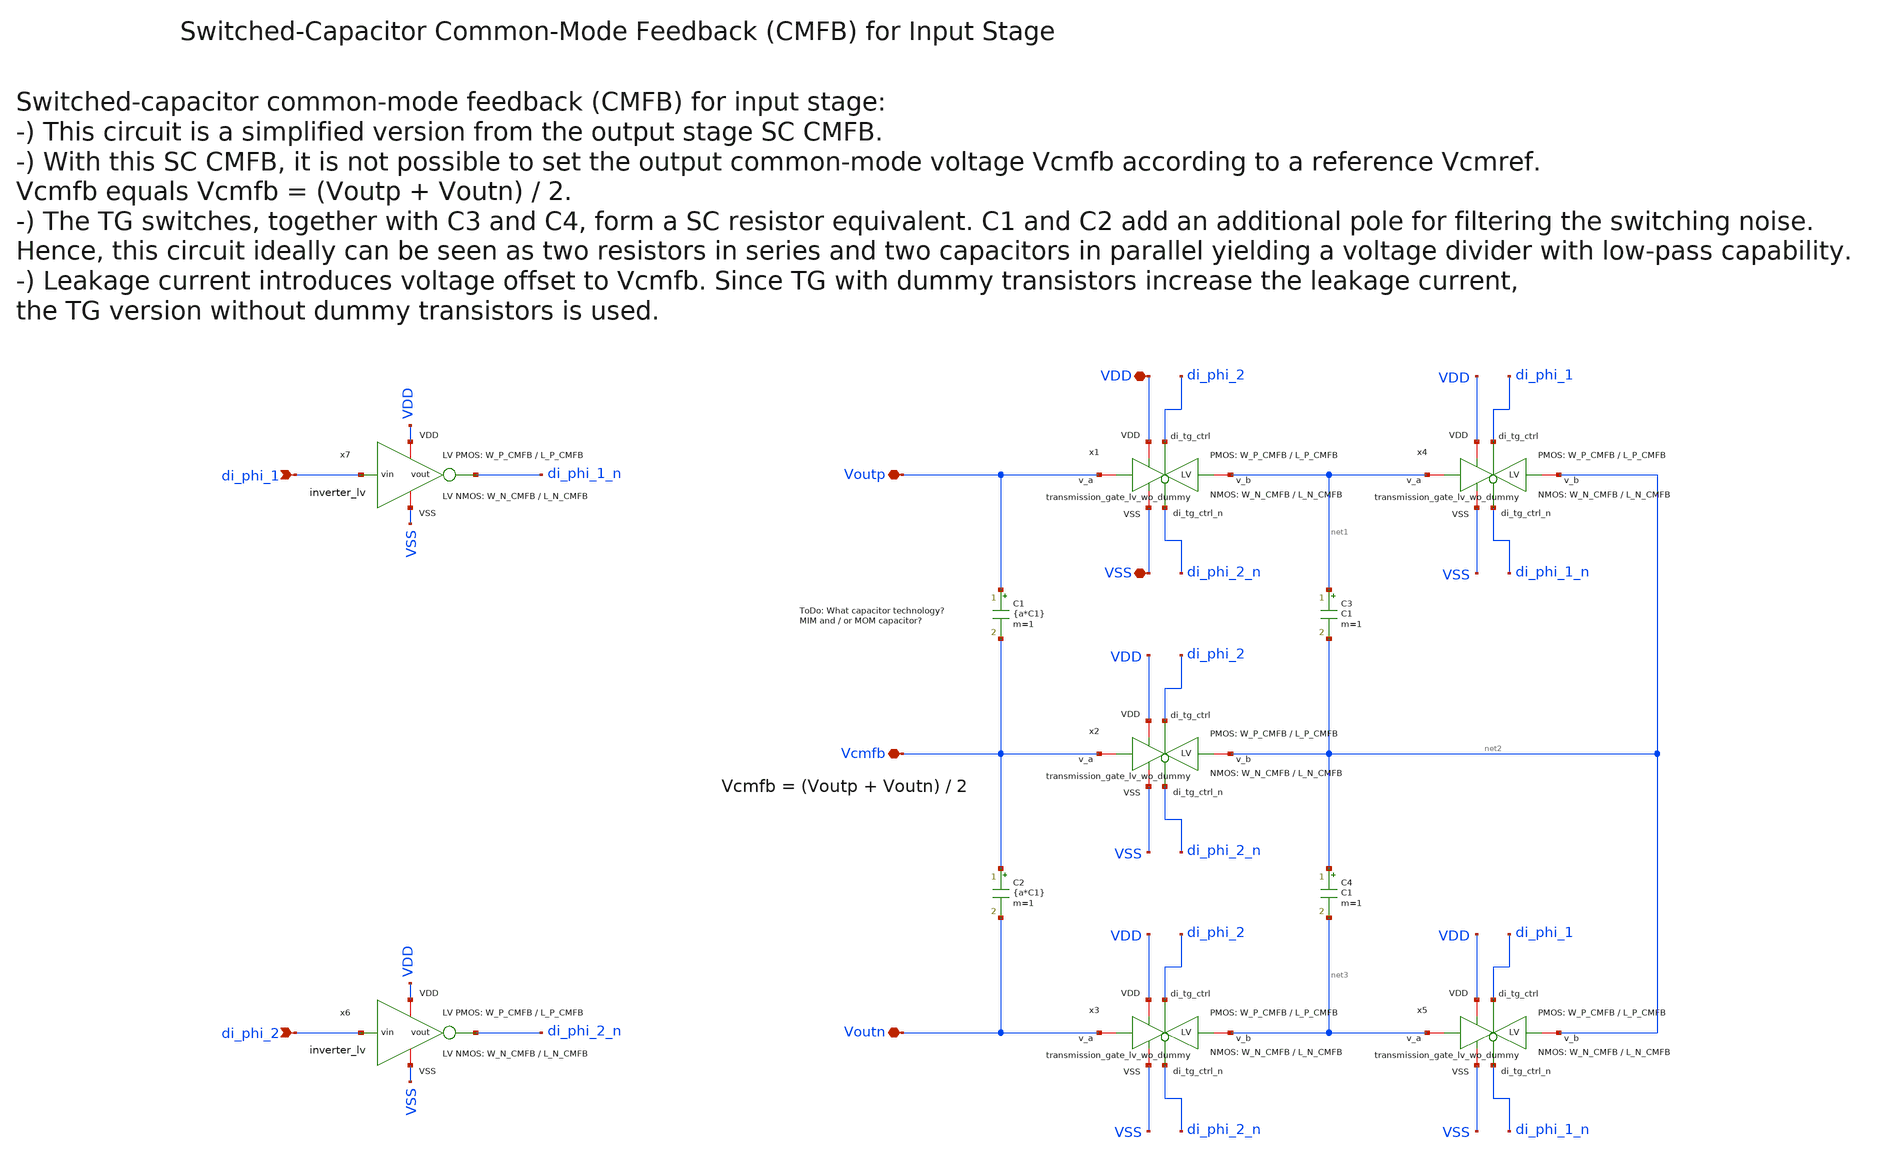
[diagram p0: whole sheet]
** sch_path: SG13G2_ATBS-ADC-main/xschem/bio_amplifier/amplifier_core/sc_cmfb/sc_cmfb_input.sch
**.subckt sc_cmfb_input VSS VDD Vcmfb Voutp Voutn di_phi_1 di_phi_2
*.iopin VSS
*.iopin VDD
*.iopin Vcmfb
*.iopin Voutp
*.iopin Voutn
*.ipin di_phi_1
*.ipin di_phi_2
x1 VDD di_phi_2 VSS net1 Voutp di_phi_2_n transmission_gate_lv_wo_dummy W_P=W_P_CMFB L_P=L_P_CMFB
+ W_N=W_N_CMFB L_N=L_N_CMFB
C1 Voutp Vcmfb {a*C1} m=1
x2 VDD di_phi_2 VSS net2 Vcmfb di_phi_2_n transmission_gate_lv_wo_dummy W_P=W_P_CMFB L_P=L_P_CMFB
+ W_N=W_N_CMFB L_N=L_N_CMFB
x3 VDD di_phi_2 VSS net3 Voutn di_phi_2_n transmission_gate_lv_wo_dummy W_P=W_P_CMFB L_P=L_P_CMFB
+ W_N=W_N_CMFB L_N=L_N_CMFB
x4 VDD di_phi_1 VSS net2 net1 di_phi_1_n transmission_gate_lv_wo_dummy W_P=W_P_CMFB L_P=L_P_CMFB
+ W_N=W_N_CMFB L_N=L_N_CMFB
x5 VDD di_phi_1 VSS net2 net3 di_phi_1_n transmission_gate_lv_wo_dummy W_P=W_P_CMFB L_P=L_P_CMFB
+ W_N=W_N_CMFB L_N=L_N_CMFB
C2 Vcmfb Voutn {a*C1} m=1
C3 net1 net2 C1 m=1
C4 net2 net3 C1 m=1
x7 VDD di_phi_1 di_phi_1_n VSS inverter_lv W_P=W_P_CMFB L_P=L_P_CMFB W_N=W_N_CMFB L_N=L_N_CMFB
x6 VDD di_phi_2 di_phi_2_n VSS inverter_lv W_P=W_P_CMFB L_P=L_P_CMFB W_N=W_N_CMFB L_N=L_N_CMFB
**.ends

* expanding   symbol:  transmission_gate/transmission_gate_lv_wo_dummy.sym # of pins=6
** sym_path: SG13G2_ATBS-ADC-main/xschem/transmission_gate/transmission_gate_lv_wo_dummy.sym
** sch_path: SG13G2_ATBS-ADC-main/xschem/transmission_gate/transmission_gate_lv_wo_dummy.sch
.subckt transmission_gate_lv_wo_dummy VDD di_tg_ctrl VSS v_b v_a di_tg_ctrl_n  W_P=1.0u L_P=0.13u
+ W_N=1.0u L_N=0.13u
*.iopin v_a
*.iopin v_b
*.iopin VDD
*.iopin VSS
*.ipin di_tg_ctrl
*.ipin di_tg_ctrl_n
XM1 v_a di_tg_ctrl v_b VSS sg13_lv_nmos w=W_N l=L_N ng=1 m=1 mm_ok=1
XM2 v_a di_tg_ctrl_n v_b VDD sg13_lv_pmos w=W_P l=L_P ng=1 m=1 mm_ok=1
.ends


* expanding   symbol:  inverter/inverter_lv.sym # of pins=4
** sym_path: SG13G2_ATBS-ADC-main/xschem/inverter/inverter_lv.sym
** sch_path: SG13G2_ATBS-ADC-main/xschem/inverter/inverter_lv.sch
.subckt inverter_lv VDD vin vout VSS  W_P=3.0u L_P=0.13u W_N=1.0u L_N=0.13u
*.ipin vin
*.iopin VDD
*.iopin VSS
*.opin vout
XM1 vout vin VDD VDD sg13_lv_pmos w=W_P l=L_P ng=1 m=1 mm_ok=1
XM2 vout vin VSS VSS sg13_lv_nmos w=W_N l=L_N ng=1 m=1 mm_ok=1
.ends

.end
